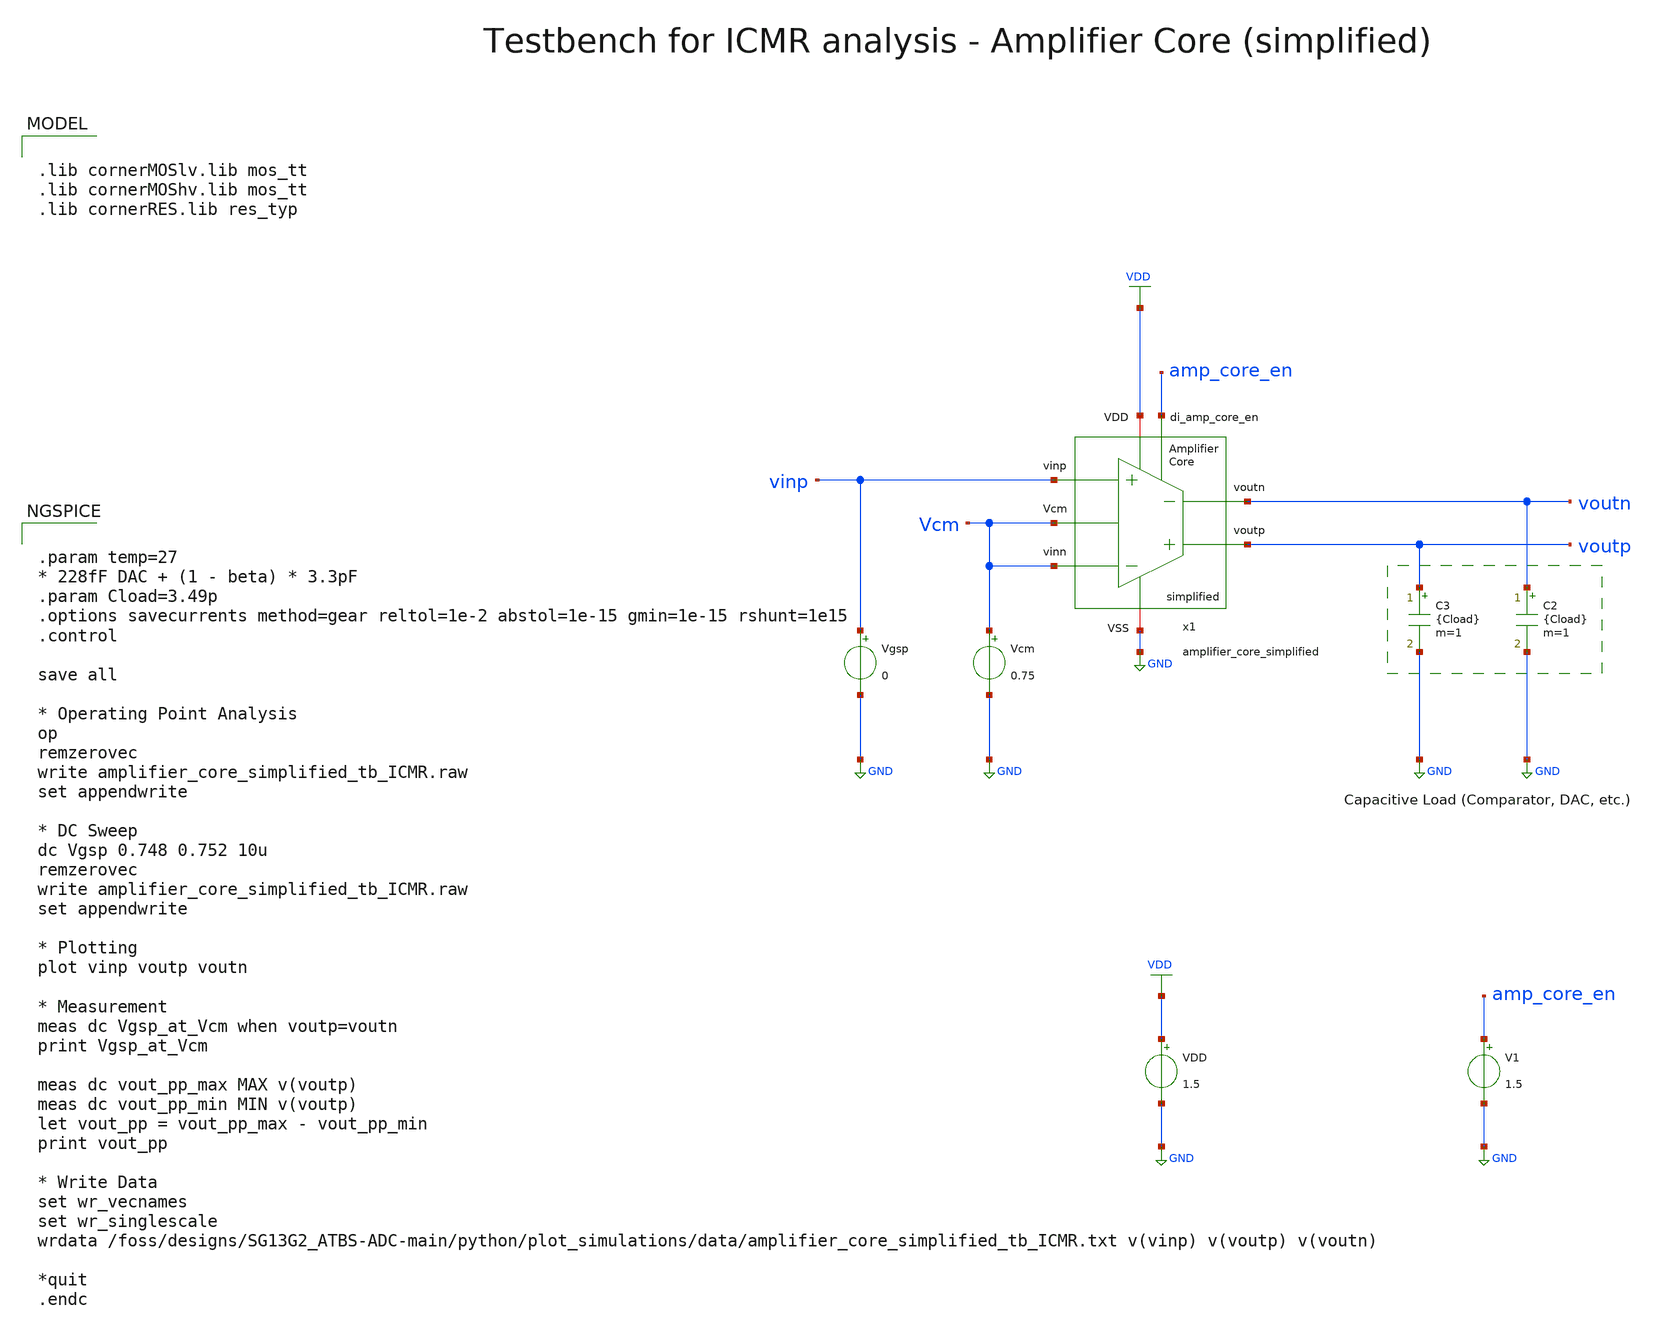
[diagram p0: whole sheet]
** sch_path: SG13G2_ATBS-ADC-main/xschem/bio_amplifier/amplifier_core/testbenches/amplifier_core_simplified_tb_ICMR.sch
**.subckt amplifier_core_simplified_tb_ICMR
VDD VDD GND 1.5
V1 amp_core_en GND 1.5
Vgsp vinp GND 0
C2 voutn GND {Cload} m=1
C3 voutp GND {Cload} m=1
Vcm Vcm GND 0.75
x1 voutp voutn amp_core_en Vcm vinp VDD GND Vcm amplifier_core_simplified
**** begin user architecture code


.param temp=27
* 228fF DAC + (1 - beta) * 3.3pF
.param Cload=3.49p
.options savecurrents method=gear reltol=1e-2 abstol=1e-15 gmin=1e-15 rshunt=1e15
.control

save all

* Operating Point Analysis
op
remzerovec
write amplifier_core_simplified_tb_ICMR.raw
set appendwrite

* DC Sweep
dc Vgsp 0.748 0.752 10u
remzerovec
write amplifier_core_simplified_tb_ICMR.raw
set appendwrite

* Plotting
plot vinp voutp voutn

* Measurement
meas dc Vgsp_at_Vcm when voutp=voutn
print Vgsp_at_Vcm

meas dc vout_pp_max MAX v(voutp)
meas dc vout_pp_min MIN v(voutp)
let vout_pp = vout_pp_max - vout_pp_min
print vout_pp

* Write Data
set wr_vecnames
set wr_singlescale
wrdata
+ /foss/designs/SG13G2_ATBS-ADC-main/python/plot_simulations/data/amplifier_core_simplified_tb_ICMR.txt v(vinp) v(voutp) v(voutn)

*quit
.endc



.lib cornerMOSlv.lib mos_tt
.lib cornerMOShv.lib mos_tt
.lib cornerRES.lib res_typ

**** end user architecture code
**.ends
.GLOBAL GND
.GLOBAL VDD
.end
